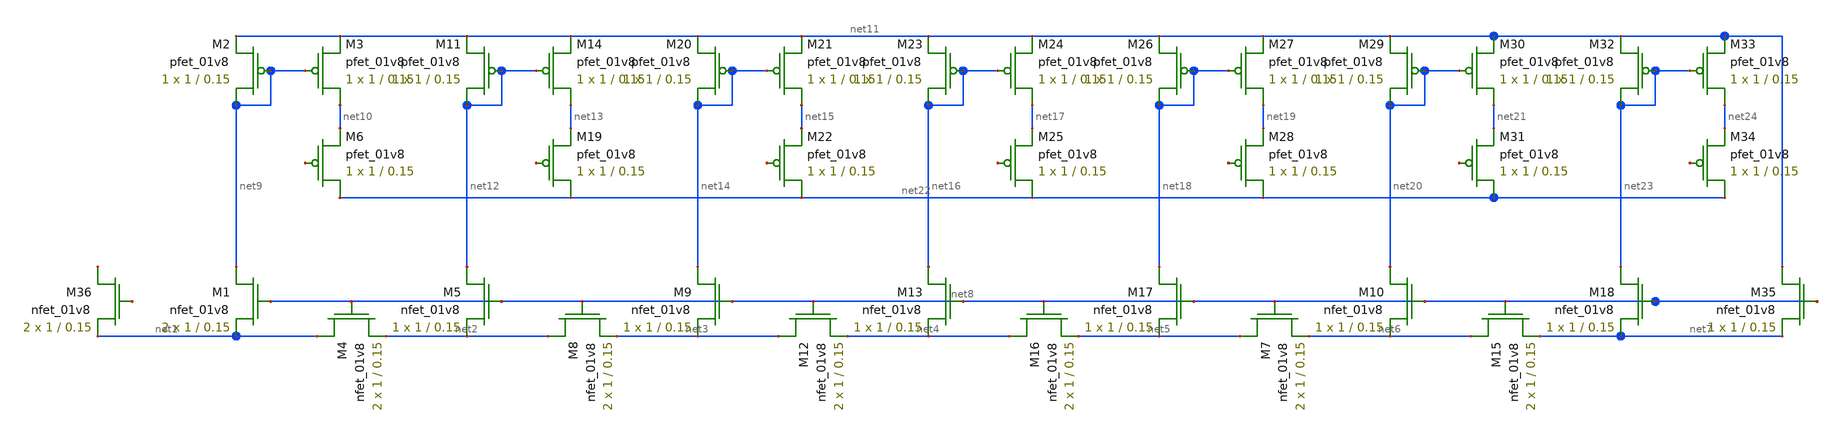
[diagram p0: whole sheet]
** sch_path: M_2M_DAC.sch
**.subckt M_2M_DAC
XM1 net9 net8 net1 GND sky130_fd_pr__nfet_01v8 L=0.15 W=1 nf=1 ad='int((nf+1)/2) * W/nf * 0.29' as='int((nf+2)/2) * W/nf * 0.29'
+ pd='2*int((nf+1)/2) * (W/nf + 0.29)' ps='2*int((nf+2)/2) * (W/nf + 0.29)' nrd='0.29 / W' nrs='0.29 / W'
+ sa=0 sb=0 sd=0 mult=2 m=2
XM4 net1 net8 net2 GND sky130_fd_pr__nfet_01v8 L=0.15 W=1 nf=1 ad='int((nf+1)/2) * W/nf * 0.29' as='int((nf+2)/2) * W/nf * 0.29'
+ pd='2*int((nf+1)/2) * (W/nf + 0.29)' ps='2*int((nf+2)/2) * (W/nf + 0.29)' nrd='0.29 / W' nrs='0.29 / W'
+ sa=0 sb=0 sd=0 mult=2 m=2
XM5 net12 net8 net2 GND sky130_fd_pr__nfet_01v8 L=0.15 W=1 nf=1 ad='int((nf+1)/2) * W/nf * 0.29' as='int((nf+2)/2) * W/nf * 0.29'
+ pd='2*int((nf+1)/2) * (W/nf + 0.29)' ps='2*int((nf+2)/2) * (W/nf + 0.29)' nrd='0.29 / W' nrs='0.29 / W'
+ sa=0 sb=0 sd=0 mult=1 m=1
XM8 net2 net8 net3 GND sky130_fd_pr__nfet_01v8 L=0.15 W=1 nf=1 ad='int((nf+1)/2) * W/nf * 0.29' as='int((nf+2)/2) * W/nf * 0.29'
+ pd='2*int((nf+1)/2) * (W/nf + 0.29)' ps='2*int((nf+2)/2) * (W/nf + 0.29)' nrd='0.29 / W' nrs='0.29 / W'
+ sa=0 sb=0 sd=0 mult=2 m=2
XM9 net14 net8 net3 GND sky130_fd_pr__nfet_01v8 L=0.15 W=1 nf=1 ad='int((nf+1)/2) * W/nf * 0.29' as='int((nf+2)/2) * W/nf * 0.29'
+ pd='2*int((nf+1)/2) * (W/nf + 0.29)' ps='2*int((nf+2)/2) * (W/nf + 0.29)' nrd='0.29 / W' nrs='0.29 / W'
+ sa=0 sb=0 sd=0 mult=1 m=1
XM12 net3 net8 net4 GND sky130_fd_pr__nfet_01v8 L=0.15 W=1 nf=1 ad='int((nf+1)/2) * W/nf * 0.29' as='int((nf+2)/2) * W/nf * 0.29'
+ pd='2*int((nf+1)/2) * (W/nf + 0.29)' ps='2*int((nf+2)/2) * (W/nf + 0.29)' nrd='0.29 / W' nrs='0.29 / W'
+ sa=0 sb=0 sd=0 mult=2 m=2
XM13 net16 net8 net4 GND sky130_fd_pr__nfet_01v8 L=0.15 W=1 nf=1 ad='int((nf+1)/2) * W/nf * 0.29' as='int((nf+2)/2) * W/nf * 0.29'
+ pd='2*int((nf+1)/2) * (W/nf + 0.29)' ps='2*int((nf+2)/2) * (W/nf + 0.29)' nrd='0.29 / W' nrs='0.29 / W'
+ sa=0 sb=0 sd=0 mult=1 m=1
XM16 net4 net8 net5 GND sky130_fd_pr__nfet_01v8 L=0.15 W=1 nf=1 ad='int((nf+1)/2) * W/nf * 0.29' as='int((nf+2)/2) * W/nf * 0.29'
+ pd='2*int((nf+1)/2) * (W/nf + 0.29)' ps='2*int((nf+2)/2) * (W/nf + 0.29)' nrd='0.29 / W' nrs='0.29 / W'
+ sa=0 sb=0 sd=0 mult=2 m=2
XM17 net18 net8 net5 GND sky130_fd_pr__nfet_01v8 L=0.15 W=1 nf=1 ad='int((nf+1)/2) * W/nf * 0.29' as='int((nf+2)/2) * W/nf * 0.29'
+ pd='2*int((nf+1)/2) * (W/nf + 0.29)' ps='2*int((nf+2)/2) * (W/nf + 0.29)' nrd='0.29 / W' nrs='0.29 / W'
+ sa=0 sb=0 sd=0 mult=1 m=1
XM7 net5 net8 net6 GND sky130_fd_pr__nfet_01v8 L=0.15 W=1 nf=1 ad='int((nf+1)/2) * W/nf * 0.29' as='int((nf+2)/2) * W/nf * 0.29'
+ pd='2*int((nf+1)/2) * (W/nf + 0.29)' ps='2*int((nf+2)/2) * (W/nf + 0.29)' nrd='0.29 / W' nrs='0.29 / W'
+ sa=0 sb=0 sd=0 mult=2 m=2
XM10 net20 net8 net6 GND sky130_fd_pr__nfet_01v8 L=0.15 W=1 nf=1 ad='int((nf+1)/2) * W/nf * 0.29' as='int((nf+2)/2) * W/nf * 0.29'
+ pd='2*int((nf+1)/2) * (W/nf + 0.29)' ps='2*int((nf+2)/2) * (W/nf + 0.29)' nrd='0.29 / W' nrs='0.29 / W'
+ sa=0 sb=0 sd=0 mult=1 m=1
XM15 net6 net8 net7 GND sky130_fd_pr__nfet_01v8 L=0.15 W=1 nf=1 ad='int((nf+1)/2) * W/nf * 0.29' as='int((nf+2)/2) * W/nf * 0.29'
+ pd='2*int((nf+1)/2) * (W/nf + 0.29)' ps='2*int((nf+2)/2) * (W/nf + 0.29)' nrd='0.29 / W' nrs='0.29 / W'
+ sa=0 sb=0 sd=0 mult=2 m=2
XM18 net23 net8 net7 GND sky130_fd_pr__nfet_01v8 L=0.15 W=1 nf=1 ad='int((nf+1)/2) * W/nf * 0.29' as='int((nf+2)/2) * W/nf * 0.29'
+ pd='2*int((nf+1)/2) * (W/nf + 0.29)' ps='2*int((nf+2)/2) * (W/nf + 0.29)' nrd='0.29 / W' nrs='0.29 / W'
+ sa=0 sb=0 sd=0 mult=1 m=1
XM2 net9 net9 net11 VDD sky130_fd_pr__pfet_01v8 L=0.15 W=1 nf=1 ad='int((nf+1)/2) * W/nf * 0.29' as='int((nf+2)/2) * W/nf * 0.29'
+ pd='2*int((nf+1)/2) * (W/nf + 0.29)' ps='2*int((nf+2)/2) * (W/nf + 0.29)' nrd='0.29 / W' nrs='0.29 / W'
+ sa=0 sb=0 sd=0 mult=1 m=1
XM3 net10 net9 net11 VDD sky130_fd_pr__pfet_01v8 L=0.15 W=1 nf=1 ad='int((nf+1)/2) * W/nf * 0.29' as='int((nf+2)/2) * W/nf * 0.29'
+ pd='2*int((nf+1)/2) * (W/nf + 0.29)' ps='2*int((nf+2)/2) * (W/nf + 0.29)' nrd='0.29 / W' nrs='0.29 / W'
+ sa=0 sb=0 sd=0 mult=1 m=1
XM6 net22 net25 net10 VDD sky130_fd_pr__pfet_01v8 L=0.15 W=1 nf=1 ad='int((nf+1)/2) * W/nf * 0.29' as='int((nf+2)/2) * W/nf * 0.29'
+ pd='2*int((nf+1)/2) * (W/nf + 0.29)' ps='2*int((nf+2)/2) * (W/nf + 0.29)' nrd='0.29 / W' nrs='0.29 / W'
+ sa=0 sb=0 sd=0 mult=1 m=1
XM11 net12 net12 net11 VDD sky130_fd_pr__pfet_01v8 L=0.15 W=1 nf=1 ad='int((nf+1)/2) * W/nf * 0.29' as='int((nf+2)/2) * W/nf * 0.29'
+ pd='2*int((nf+1)/2) * (W/nf + 0.29)' ps='2*int((nf+2)/2) * (W/nf + 0.29)' nrd='0.29 / W' nrs='0.29 / W'
+ sa=0 sb=0 sd=0 mult=1 m=1
XM14 net13 net12 net11 VDD sky130_fd_pr__pfet_01v8 L=0.15 W=1 nf=1 ad='int((nf+1)/2) * W/nf * 0.29' as='int((nf+2)/2) * W/nf * 0.29'
+ pd='2*int((nf+1)/2) * (W/nf + 0.29)' ps='2*int((nf+2)/2) * (W/nf + 0.29)' nrd='0.29 / W' nrs='0.29 / W'
+ sa=0 sb=0 sd=0 mult=1 m=1
XM19 net22 net26 net13 VDD sky130_fd_pr__pfet_01v8 L=0.15 W=1 nf=1 ad='int((nf+1)/2) * W/nf * 0.29' as='int((nf+2)/2) * W/nf * 0.29'
+ pd='2*int((nf+1)/2) * (W/nf + 0.29)' ps='2*int((nf+2)/2) * (W/nf + 0.29)' nrd='0.29 / W' nrs='0.29 / W'
+ sa=0 sb=0 sd=0 mult=1 m=1
XM20 net14 net14 net11 VDD sky130_fd_pr__pfet_01v8 L=0.15 W=1 nf=1 ad='int((nf+1)/2) * W/nf * 0.29' as='int((nf+2)/2) * W/nf * 0.29'
+ pd='2*int((nf+1)/2) * (W/nf + 0.29)' ps='2*int((nf+2)/2) * (W/nf + 0.29)' nrd='0.29 / W' nrs='0.29 / W'
+ sa=0 sb=0 sd=0 mult=1 m=1
XM21 net15 net14 net11 VDD sky130_fd_pr__pfet_01v8 L=0.15 W=1 nf=1 ad='int((nf+1)/2) * W/nf * 0.29' as='int((nf+2)/2) * W/nf * 0.29'
+ pd='2*int((nf+1)/2) * (W/nf + 0.29)' ps='2*int((nf+2)/2) * (W/nf + 0.29)' nrd='0.29 / W' nrs='0.29 / W'
+ sa=0 sb=0 sd=0 mult=1 m=1
XM22 net22 net27 net15 VDD sky130_fd_pr__pfet_01v8 L=0.15 W=1 nf=1 ad='int((nf+1)/2) * W/nf * 0.29' as='int((nf+2)/2) * W/nf * 0.29'
+ pd='2*int((nf+1)/2) * (W/nf + 0.29)' ps='2*int((nf+2)/2) * (W/nf + 0.29)' nrd='0.29 / W' nrs='0.29 / W'
+ sa=0 sb=0 sd=0 mult=1 m=1
XM23 net16 net16 net11 VDD sky130_fd_pr__pfet_01v8 L=0.15 W=1 nf=1 ad='int((nf+1)/2) * W/nf * 0.29' as='int((nf+2)/2) * W/nf * 0.29'
+ pd='2*int((nf+1)/2) * (W/nf + 0.29)' ps='2*int((nf+2)/2) * (W/nf + 0.29)' nrd='0.29 / W' nrs='0.29 / W'
+ sa=0 sb=0 sd=0 mult=1 m=1
XM24 net17 net16 net11 VDD sky130_fd_pr__pfet_01v8 L=0.15 W=1 nf=1 ad='int((nf+1)/2) * W/nf * 0.29' as='int((nf+2)/2) * W/nf * 0.29'
+ pd='2*int((nf+1)/2) * (W/nf + 0.29)' ps='2*int((nf+2)/2) * (W/nf + 0.29)' nrd='0.29 / W' nrs='0.29 / W'
+ sa=0 sb=0 sd=0 mult=1 m=1
XM25 net22 net28 net17 VDD sky130_fd_pr__pfet_01v8 L=0.15 W=1 nf=1 ad='int((nf+1)/2) * W/nf * 0.29' as='int((nf+2)/2) * W/nf * 0.29'
+ pd='2*int((nf+1)/2) * (W/nf + 0.29)' ps='2*int((nf+2)/2) * (W/nf + 0.29)' nrd='0.29 / W' nrs='0.29 / W'
+ sa=0 sb=0 sd=0 mult=1 m=1
XM26 net18 net18 net11 VDD sky130_fd_pr__pfet_01v8 L=0.15 W=1 nf=1 ad='int((nf+1)/2) * W/nf * 0.29' as='int((nf+2)/2) * W/nf * 0.29'
+ pd='2*int((nf+1)/2) * (W/nf + 0.29)' ps='2*int((nf+2)/2) * (W/nf + 0.29)' nrd='0.29 / W' nrs='0.29 / W'
+ sa=0 sb=0 sd=0 mult=1 m=1
XM27 net19 net18 net11 VDD sky130_fd_pr__pfet_01v8 L=0.15 W=1 nf=1 ad='int((nf+1)/2) * W/nf * 0.29' as='int((nf+2)/2) * W/nf * 0.29'
+ pd='2*int((nf+1)/2) * (W/nf + 0.29)' ps='2*int((nf+2)/2) * (W/nf + 0.29)' nrd='0.29 / W' nrs='0.29 / W'
+ sa=0 sb=0 sd=0 mult=1 m=1
XM28 net22 net29 net19 VDD sky130_fd_pr__pfet_01v8 L=0.15 W=1 nf=1 ad='int((nf+1)/2) * W/nf * 0.29' as='int((nf+2)/2) * W/nf * 0.29'
+ pd='2*int((nf+1)/2) * (W/nf + 0.29)' ps='2*int((nf+2)/2) * (W/nf + 0.29)' nrd='0.29 / W' nrs='0.29 / W'
+ sa=0 sb=0 sd=0 mult=1 m=1
XM29 net20 net20 net11 VDD sky130_fd_pr__pfet_01v8 L=0.15 W=1 nf=1 ad='int((nf+1)/2) * W/nf * 0.29' as='int((nf+2)/2) * W/nf * 0.29'
+ pd='2*int((nf+1)/2) * (W/nf + 0.29)' ps='2*int((nf+2)/2) * (W/nf + 0.29)' nrd='0.29 / W' nrs='0.29 / W'
+ sa=0 sb=0 sd=0 mult=1 m=1
XM30 net21 net20 net11 VDD sky130_fd_pr__pfet_01v8 L=0.15 W=1 nf=1 ad='int((nf+1)/2) * W/nf * 0.29' as='int((nf+2)/2) * W/nf * 0.29'
+ pd='2*int((nf+1)/2) * (W/nf + 0.29)' ps='2*int((nf+2)/2) * (W/nf + 0.29)' nrd='0.29 / W' nrs='0.29 / W'
+ sa=0 sb=0 sd=0 mult=1 m=1
XM31 net22 net30 net21 VDD sky130_fd_pr__pfet_01v8 L=0.15 W=1 nf=1 ad='int((nf+1)/2) * W/nf * 0.29' as='int((nf+2)/2) * W/nf * 0.29'
+ pd='2*int((nf+1)/2) * (W/nf + 0.29)' ps='2*int((nf+2)/2) * (W/nf + 0.29)' nrd='0.29 / W' nrs='0.29 / W'
+ sa=0 sb=0 sd=0 mult=1 m=1
XM32 net23 net23 net11 VDD sky130_fd_pr__pfet_01v8 L=0.15 W=1 nf=1 ad='int((nf+1)/2) * W/nf * 0.29' as='int((nf+2)/2) * W/nf * 0.29'
+ pd='2*int((nf+1)/2) * (W/nf + 0.29)' ps='2*int((nf+2)/2) * (W/nf + 0.29)' nrd='0.29 / W' nrs='0.29 / W'
+ sa=0 sb=0 sd=0 mult=1 m=1
XM33 net24 net23 net11 VDD sky130_fd_pr__pfet_01v8 L=0.15 W=1 nf=1 ad='int((nf+1)/2) * W/nf * 0.29' as='int((nf+2)/2) * W/nf * 0.29'
+ pd='2*int((nf+1)/2) * (W/nf + 0.29)' ps='2*int((nf+2)/2) * (W/nf + 0.29)' nrd='0.29 / W' nrs='0.29 / W'
+ sa=0 sb=0 sd=0 mult=1 m=1
XM34 net22 net31 net24 VDD sky130_fd_pr__pfet_01v8 L=0.15 W=1 nf=1 ad='int((nf+1)/2) * W/nf * 0.29' as='int((nf+2)/2) * W/nf * 0.29'
+ pd='2*int((nf+1)/2) * (W/nf + 0.29)' ps='2*int((nf+2)/2) * (W/nf + 0.29)' nrd='0.29 / W' nrs='0.29 / W'
+ sa=0 sb=0 sd=0 mult=1 m=1
XM35 net11 net8 net7 GND sky130_fd_pr__nfet_01v8 L=0.15 W=1 nf=1 ad='int((nf+1)/2) * W/nf * 0.29' as='int((nf+2)/2) * W/nf * 0.29'
+ pd='2*int((nf+1)/2) * (W/nf + 0.29)' ps='2*int((nf+2)/2) * (W/nf + 0.29)' nrd='0.29 / W' nrs='0.29 / W'
+ sa=0 sb=0 sd=0 mult=1 m=1
XM36 net32 net33 net1 GND sky130_fd_pr__nfet_01v8 L=0.15 W=1 nf=1 ad='int((nf+1)/2) * W/nf * 0.29' as='int((nf+2)/2) * W/nf * 0.29'
+ pd='2*int((nf+1)/2) * (W/nf + 0.29)' ps='2*int((nf+2)/2) * (W/nf + 0.29)' nrd='0.29 / W' nrs='0.29 / W'
+ sa=0 sb=0 sd=0 mult=2 m=2
**.ends
.end
